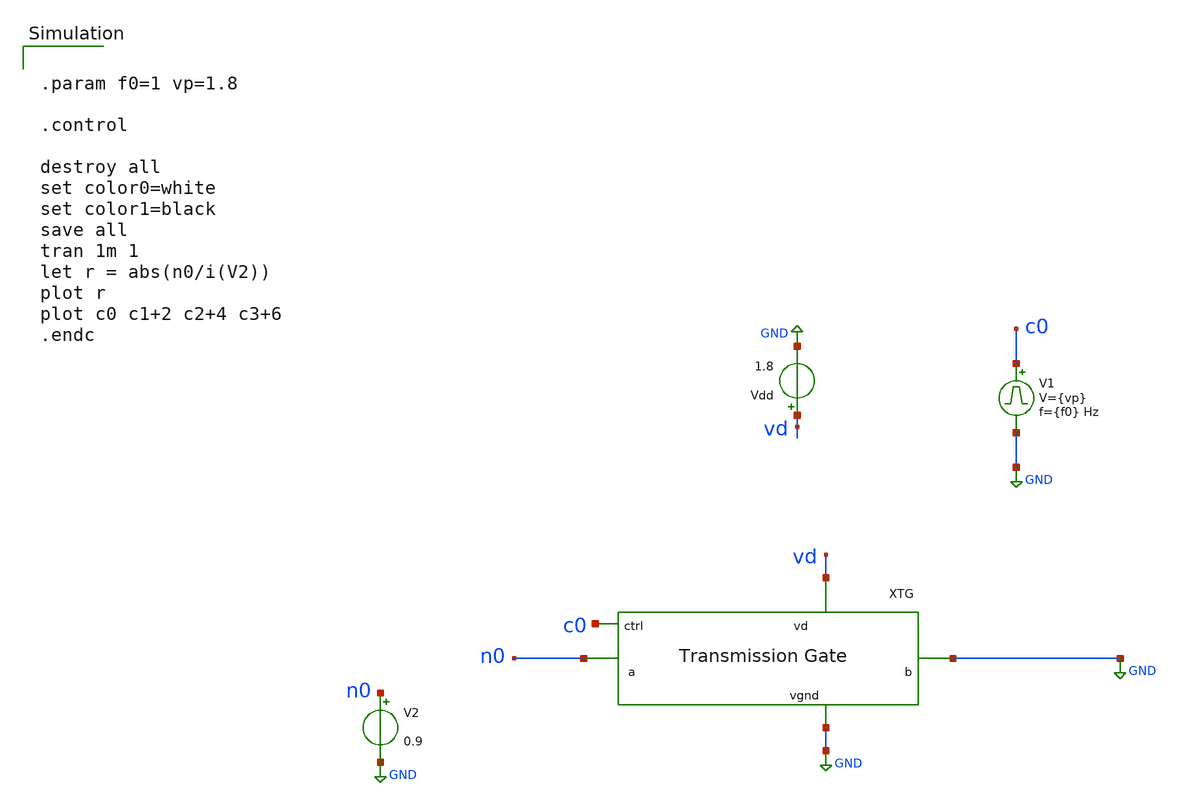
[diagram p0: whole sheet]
** sch_path: xschem/tg-tb.sch
**.subckt tg-tb
Vdd vd GND 1.8
V1 c0 GND pulse 0 {vp} '0.495/ {f0} ' '0.01/{f0} ' '0.01/{f0} ' '0.49/{f0} ' '1/{f0} '
V2 n0 GND 0.9
x2 c0 vd GND GND n0 tg
**** begin user architecture code


.param f0=1 vp=1.8

.control

destroy all
set color0=white
set color1=black
save all
tran 1m 1
let r = abs(n0/i(V2))
plot r
plot c0 c1+2 c2+4 c3+6
.endc

 .lib $::SKYWATER_MODELS/sky130.lib.spice tt
.include $::SKYWATER_STDCELLS/sky130_fd_sc_hd.spice

**** end user architecture code
**.ends

* expanding   symbol:  projects/dpga-ieee-sscs-contest/xschem/tg.sym # of pins=5
** sym_path: projects/dpga-ieee-sscs-contest/xschem/tg.sym
** sch_path: projects/dpga-ieee-sscs-contest/xschem/tg.sch
.subckt tg ctrl vd b vgnd a
*.iopin vd
*.iopin vgnd
*.iopin b
*.iopin a
*.ipin ctrl
XM2 b nctrl a vd sky130_fd_pr__pfet_01v8 L=0.15 W=60 nf=12 ad='int((nf+1)/2) * W/nf * 0.29' as='int((nf+2)/2) * W/nf * 0.29'
+ pd='2*int((nf+1)/2) * (W/nf + 0.29)' ps='2*int((nf+2)/2) * (W/nf + 0.29)' nrd='0.29 / W' nrs='0.29 / W'
+ sa=0 sb=0 sd=0 mult=1 m=1
XM1 a ctrl b vgnd sky130_fd_pr__nfet_01v8 L=0.15 W=60 nf=12 ad='int((nf+1)/2) * W/nf * 0.29' as='int((nf+2)/2) * W/nf * 0.29'
+ pd='2*int((nf+1)/2) * (W/nf + 0.29)' ps='2*int((nf+2)/2) * (W/nf + 0.29)' nrd='0.29 / W' nrs='0.29 / W'
+ sa=0 sb=0 sd=0 mult=1 m=1
XM3 nctrl ctrl vgnd vgnd sky130_fd_pr__nfet_01v8 L=0.15 W=1 nf=1 ad='int((nf+1)/2) * W/nf * 0.29' as='int((nf+2)/2) * W/nf * 0.29'
+ pd='2*int((nf+1)/2) * (W/nf + 0.29)' ps='2*int((nf+2)/2) * (W/nf + 0.29)' nrd='0.29 / W' nrs='0.29 / W'
+ sa=0 sb=0 sd=0 mult=1 m=1
XM4 nctrl ctrl vd vd sky130_fd_pr__pfet_01v8 L=0.15 W=3 nf=1 ad='int((nf+1)/2) * W/nf * 0.29' as='int((nf+2)/2) * W/nf * 0.29'
+ pd='2*int((nf+1)/2) * (W/nf + 0.29)' ps='2*int((nf+2)/2) * (W/nf + 0.29)' nrd='0.29 / W' nrs='0.29 / W'
+ sa=0 sb=0 sd=0 mult=1 m=1
.ends

.GLOBAL GND
.end
